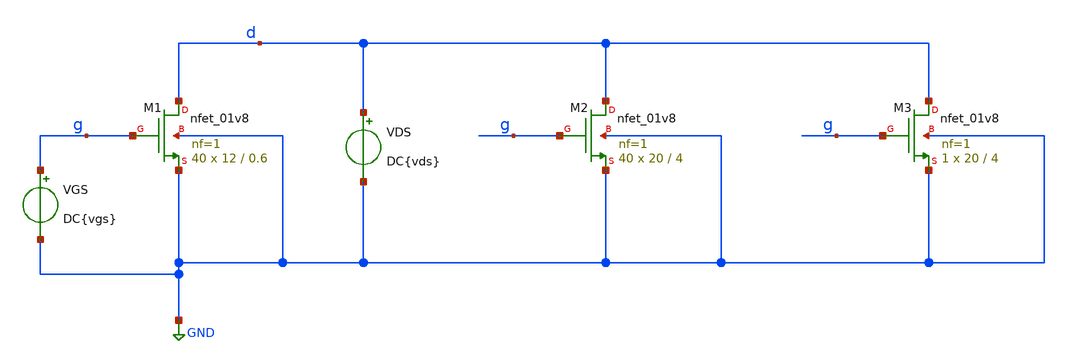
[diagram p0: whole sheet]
** sch_path: tp1/tp1_1.sch
* Copyright 2021 Stefan Frederik Schippers
**.subckt tp1_1
XM1 d g GND GND sky130_fd_pr__nfet_01v8 L=0.6 W=12 nf=1 ad='int((nf+1)/2) * W/nf * 0.29' as='int((nf+2)/2) * W/nf * 0.29'
+ pd='2*int((nf+1)/2) * (W/nf + 0.29)' ps='2*int((nf+2)/2) * (W/nf + 0.29)' nrd='0.29 / W' nrs='0.29 / W'
+ sa=0 sb=0 sd=0 mult=40 m=40
VGS g GND DC{vgs}
VDS d GND DC{vds}
XM3 d g GND GND sky130_fd_pr__nfet_01v8 L=4 W=20 nf=1 ad='int((nf+1)/2) * W/nf * 0.29' as='int((nf+2)/2) * W/nf * 0.29'
+ pd='2*int((nf+1)/2) * (W/nf + 0.29)' ps='2*int((nf+2)/2) * (W/nf + 0.29)' nrd='0.29 / W' nrs='0.29 / W'
+ sa=0 sb=0 sd=0 mult=1 m=1
XM2 d g GND GND sky130_fd_pr__nfet_01v8 L=4 W=20 nf=1 ad='int((nf+1)/2) * W/nf * 0.29' as='int((nf+2)/2) * W/nf * 0.29'
+ pd='2*int((nf+1)/2) * (W/nf + 0.29)' ps='2*int((nf+2)/2) * (W/nf + 0.29)' nrd='0.29 / W' nrs='0.29 / W'
+ sa=0 sb=0 sd=0 mult=40 m=40
**** begin user architecture code



* Parameters
.param vds = 1.8
.param vgs = 0.9
.options TEMPS = 27.0

* Models
*.lib ~/skywater/skywater-pdk/libraries/sky130_fd_pr_ngspice/latest/models/corners/sky130.lib TT
.lib $PDK_ROOT/sky130A/libs.tech/ngspice/sky130.lib.spice tt
* Data to save
.save all  @M.XM1.msky130_fd_pr__nfet_01v8[id]  @M.XM1.msky130_fd_pr__nfet_01v8[gm]  @M.XM1.msky130_fd_pr__nfet_01v8[vth]  @M.XM1.msky130_fd_pr__nfet_01v8[vds]  @M.XM1.msky130_fd_pr__nfet_01v8[vdsat]  @M.XM1.msky130_fd_pr__nfet_01v8[vgs]  @M.XM1.msky130_fd_pr__nfet_01v8[cgg]  @M.XM2.msky130_fd_pr__nfet_01v8[id]  @M.XM2.msky130_fd_pr__nfet_01v8[gm]  @M.XM2.msky130_fd_pr__nfet_01v8[vth]  @M.XM2.msky130_fd_pr__nfet_01v8[vds]  @M.XM2.msky130_fd_pr__nfet_01v8[vdsat]  @M.XM2.msky130_fd_pr__nfet_01v8[vgs]  @M.XM3.msky130_fd_pr__nfet_01v8[id]  @M.XM3.msky130_fd_pr__nfet_01v8[gm]  @M.XM3.msky130_fd_pr__nfet_01v8[vth]  @M.XM3.msky130_fd_pr__nfet_01v8[vds]  @M.XM3.msky130_fd_pr__nfet_01v8[vdsat]  @M.XM3.msky130_fd_pr__nfet_01v8[vgs]


* Simulation
.control
  dc VDS 0 1.8 0.01 VGS 0 1.8 0.3
  setplot dc1
  plot @M.XM1.msky130_fd_pr__nfet_01v8[id] @M.XM3.msky130_fd_pr__nfet_01v8[id] ylabel Id xlabel Vds title
+ 'Id vs Vds vs Vgs'
  set filetype = ascii
  write tp1_1_dc1.raw

  reset
  dc VGS 0 1.8 0.01
  setplot dc2
  plot @M.XM1.msky130_fd_pr__nfet_01v8[id] @M.XM2.msky130_fd_pr__nfet_01v8[id]
+ @M.XM3.msky130_fd_pr__nfet_01v8[id] ylabel Id xlabel Vgs
  plot @M.XM1.msky130_fd_pr__nfet_01v8[id] @M.XM2.msky130_fd_pr__nfet_01v8[id]
+ @M.XM3.msky130_fd_pr__nfet_01v8[id] ylog ylabel log(Id) xlabel Vgs
  plot @M.XM1.msky130_fd_pr__nfet_01v8[gm]/@M.XM1.msky130_fd_pr__nfet_01v8[id] vs
+ @M.XM1.msky130_fd_pr__nfet_01v8[id] xlog ylabel gm/Id xlabel Id
  plot @M.XM1.msky130_fd_pr__nfet_01v8[gm]/@M.XM1.msky130_fd_pr__nfet_01v8[id] vs
+ @M.XM1.msky130_fd_pr__nfet_01v8[vgs] ylabel gm/Id xlabel Vgs
  plot @M.XM1.msky130_fd_pr__nfet_01v8[gm] vs @M.XM1.msky130_fd_pr__nfet_01v8[id] xlog ylabel gm/Id
+ xlabel Id
  plot @M.XM1.msky130_fd_pr__nfet_01v8[gm] vs @M.XM1.msky130_fd_pr__nfet_01v8[vgs] ylabel gm/Id
+ xlabel Vgs
  set filetype = ascii
  write tp1_1_dc2.raw

  alterparam vds = 0
  reset
  dc VGS -1.8 1.8 0.01
  setplot dc3
  plot @M.XM1.msky130_fd_pr__nfet_01v8[cgg] ylabel Cgg xlabel Vgs
  set filetype = ascii
  write tp1_1_dc3.raw

  reset
  unset filetype
  op
  save all
  write tp1_1.raw

.endc

.end


**** end user architecture code
**.ends
.GLOBAL GND
.end
